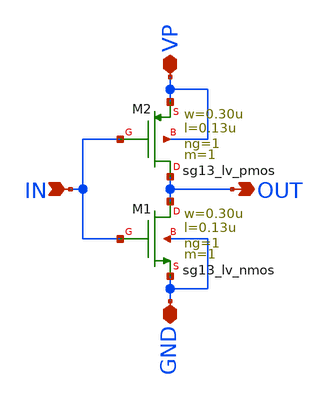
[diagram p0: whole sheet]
** sch_path: schematics/divider/schematics/inverter_x2.sch
**.subckt inverter_x2 IN VP OUT GND
*.ipin IN
*.iopin VP
*.opin OUT
*.iopin GND
XM1 OUT IN GND GND sg13_lv_nmos w=0.30u l=0.13u ng=1 m=1 mm_ok=1
XM2 OUT IN VP VP sg13_lv_pmos w=0.30u l=0.13u ng=1 m=1 mm_ok=1
**.ends
.end
